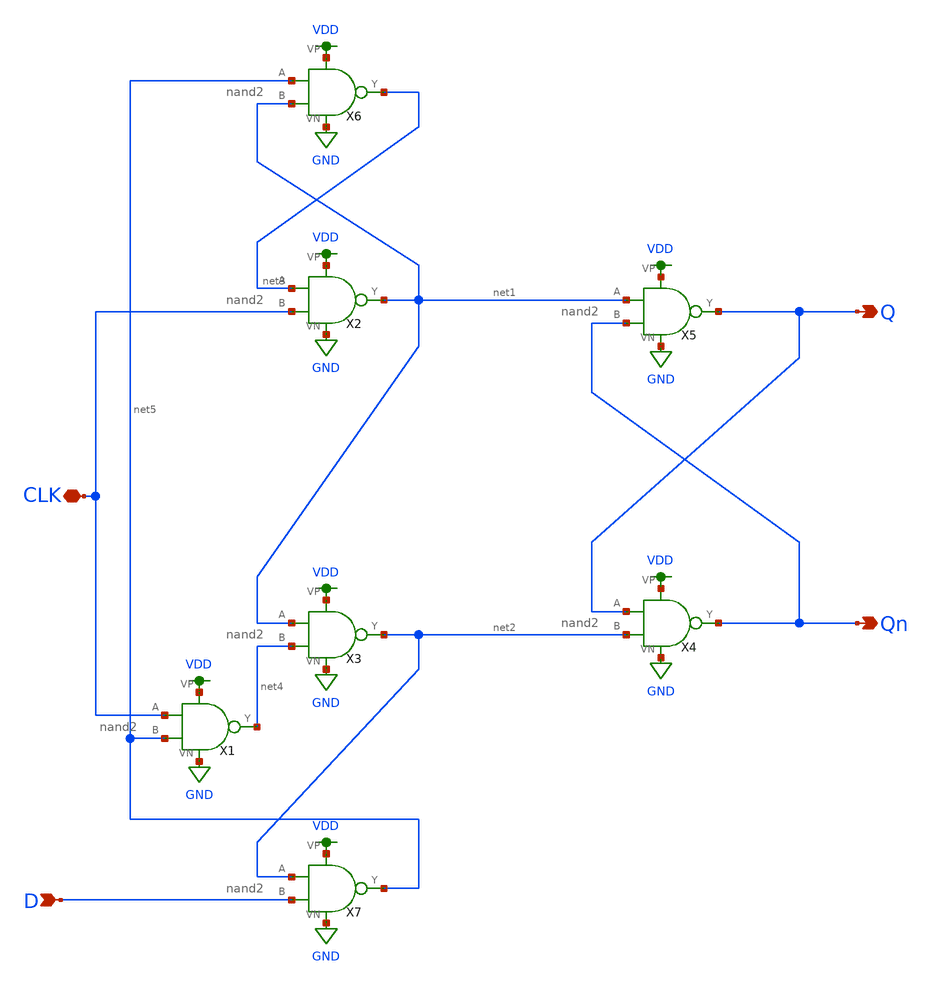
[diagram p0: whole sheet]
** sch_path: schematic/dff_sr.sch
**.subckt dff_sr D CLK Qn Q
*.ipin D
*.iopin CLK
*.opin Qn
*.opin Q
X2 net3 CLK net1 VDD GND nand2
X3 net1 net4 net2 VDD GND nand2
X4 Q net2 Qn VDD GND nand2
X5 net1 Qn Q VDD GND nand2
X1 CLK net5 net4 VDD GND nand2
X6 net5 net1 net3 VDD GND nand2
X7 net2 D net5 VDD GND nand2
**.ends

* expanding   symbol:  /home/madvlsi/Documents/MADVLSI-Final_Project/schematic/nand2.sym # of pins=5
** sym_path: schematic/nand2.sym
** sch_path: schematic/nand2.sch
.subckt nand2 A B Y VP VN
*.ipin A
*.opin Y
*.ipin B
*.iopin VP
*.iopin VP
*.iopin VN
*.iopin VN
XM1 Y A VP VP sky130_fd_pr__pfet_01v8 L=0.15 W=2 nf=1 ad='int((nf+1)/2) * W/nf * 0.29' as='int((nf+2)/2) * W/nf * 0.29'
+ pd='2*int((nf+1)/2) * (W/nf + 0.29)' ps='2*int((nf+2)/2) * (W/nf + 0.29)' nrd='0.29 / W' nrs='0.29 / W'
+ sa=0 sb=0 sd=0 mult=1 m=1
XM2 VP B Y VP sky130_fd_pr__pfet_01v8 L=0.15 W=2 nf=1 ad='int((nf+1)/2) * W/nf * 0.29' as='int((nf+2)/2) * W/nf * 0.29'
+ pd='2*int((nf+1)/2) * (W/nf + 0.29)' ps='2*int((nf+2)/2) * (W/nf + 0.29)' nrd='0.29 / W' nrs='0.29 / W'
+ sa=0 sb=0 sd=0 mult=1 m=1
XM3 net1 B Y VN sky130_fd_pr__nfet_01v8 L=0.15 W=2 nf=1 ad='int((nf+1)/2) * W/nf * 0.29' as='int((nf+2)/2) * W/nf * 0.29'
+ pd='2*int((nf+1)/2) * (W/nf + 0.29)' ps='2*int((nf+2)/2) * (W/nf + 0.29)' nrd='0.29 / W' nrs='0.29 / W'
+ sa=0 sb=0 sd=0 mult=1 m=1
XM4 net1 A VN VN sky130_fd_pr__nfet_01v8 L=0.15 W=2 nf=1 ad='int((nf+1)/2) * W/nf * 0.29' as='int((nf+2)/2) * W/nf * 0.29'
+ pd='2*int((nf+1)/2) * (W/nf + 0.29)' ps='2*int((nf+2)/2) * (W/nf + 0.29)' nrd='0.29 / W' nrs='0.29 / W'
+ sa=0 sb=0 sd=0 mult=1 m=1
.ends

.GLOBAL VDD
.GLOBAL GND
.end
